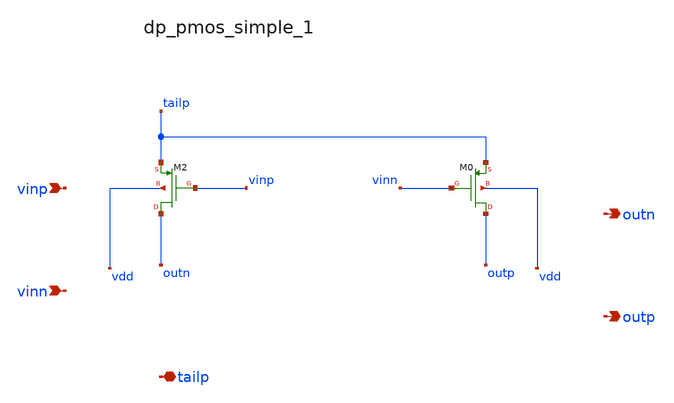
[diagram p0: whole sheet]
** sch_path: analog-db/raw/amp_024_smcnr/hier/blocks/dp_pmos_simple_1.sch
**.subckt dp_pmos_simple_1 vinp vinn tailp outn outp
*.ipin vinp
*.ipin vinn
*.iopin tailp
*.opin outn
*.opin outp
XM0 outp vinn tailp vdd sg13_lv_pmos w=x_dut_xm0_w l=x_dut_xm0_l ng=1 m=x_dut_xm0_m
XM2 outn vinp tailp vdd sg13_lv_pmos w=x_dut_xm2_w l=x_dut_xm2_l ng=1 m=x_dut_xm2_m
**.ends
.end
